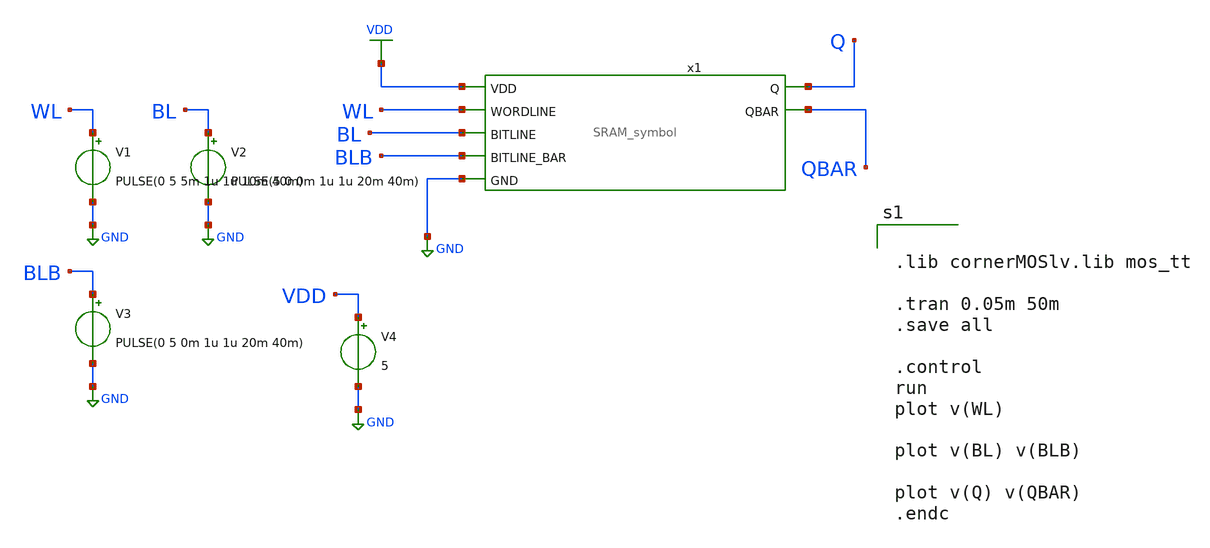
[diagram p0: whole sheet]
** sch_path: projetofinal/shared/sram_sim.sch
**.subckt sram_sim
V1 WL GND PULSE(0 5 5m 1u 1u 10m 40m)
V2 BL GND PULSE(5 0 0m 1u 1u 20m 40m)
V3 BLB GND PULSE(0 5 0m 1u 1u 20m 40m)
x1 VDD WL BL BLB Q QBAR GND SRAM_symbol
V4 VDD GND 5
**** begin user architecture code


.lib cornerMOSlv.lib mos_tt

.tran 0.05m 50m
.save all

.control
run
plot v(WL)

plot v(BL) v(BLB)

plot v(Q) v(QBAR)
.endc


**** end user architecture code
**.ends

* expanding   symbol:  /home/designer/shared/SRAM_symbol.sym # of pins=7
** sym_path: projetofinal/shared/schematic_sram/SRAM_symbol.sym
** sch_path: projetofinal/shared/schematic_sram/SRAM_symbol.sch
.subckt SRAM_symbol VDD WORDLINE BITLINE BITLINE_BAR Q QBAR GND
*.ipin BITLINE
*.opin Q
*.ipin BITLINE_BAR
*.ipin VDD
*.ipin WORDLINE
*.ipin GND
*.opin QBAR
XM5 Q QBAR VDD VDD sg13_lv_pmos w=0.15u l=0.13u ng=1 m=1 mm_ok=1
XM9 Q QBAR GND GND sg13_lv_nmos w=0.15u l=0.13u ng=1 m=1 mm_ok=1
XM8 QBAR Q VDD VDD sg13_lv_pmos w=0.15u l=0.13u ng=1 m=1 mm_ok=1
XM1 GND Q QBAR GND sg13_lv_nmos w=0.15u l=0.13u ng=1 m=1 mm_ok=1
XM2 Q WORDLINE BITLINE GND sg13_lv_nmos w=0.15u l=0.13u ng=1 m=1 mm_ok=1
XM3 QBAR WORDLINE BITLINE_BAR GND sg13_lv_nmos w=0.15u l=0.13u ng=1 m=1 mm_ok=1
.ends

.GLOBAL VDD
.GLOBAL GND
.end
